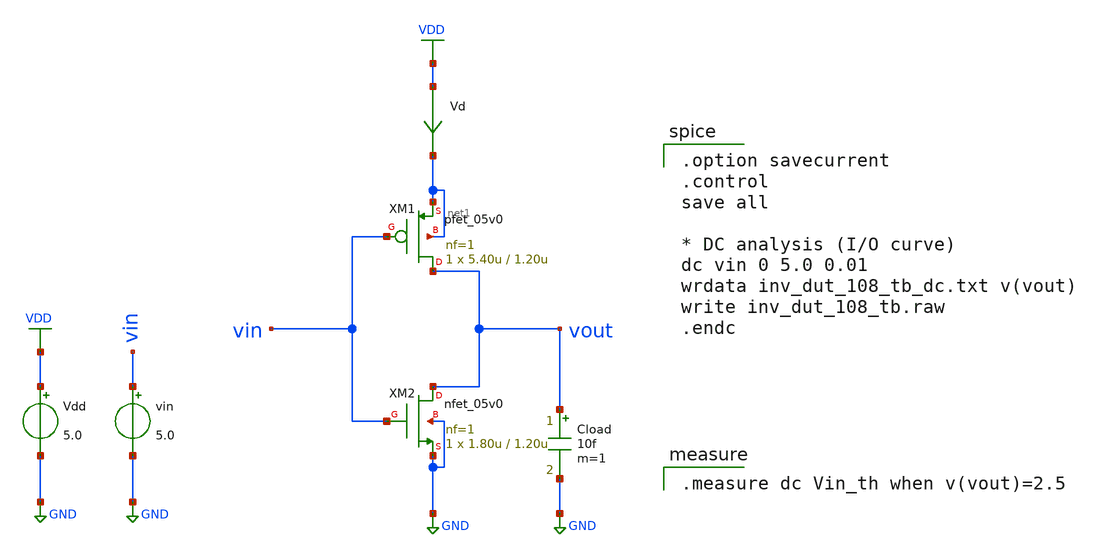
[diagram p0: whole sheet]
** sch_path: inv_dut_108_tb.sch
**.subckt inv_dut_108_tb
Vdd VDD GND 5.0
vin vin GND 5.0
Vd VDD net1 0
.save i(vd)
Cload vout GND 10f m=1
XM1 vout vin net1 net1 pfet_05v0 L=1.20u W=5.40u nf=1 ad='int((nf+1)/2) * W/nf * 0.18u' as='int((nf+2)/2) * W/nf * 0.18u'
+ pd='2*int((nf+1)/2) * (W/nf + 0.18u)' ps='2*int((nf+2)/2) * (W/nf + 0.18u)' nrd='0.18u / W' nrs='0.18u / W'
+ sa=0 sb=0 sd=0 m=1
XM2 vout vin GND GND nfet_05v0 L=1.20u W=1.80u nf=1 ad='int((nf+1)/2) * W/nf * 0.18u' as='int((nf+2)/2) * W/nf * 0.18u'
+ pd='2*int((nf+1)/2) * (W/nf + 0.18u)' ps='2*int((nf+2)/2) * (W/nf + 0.18u)' nrd='0.18u / W' nrs='0.18u / W'
+ sa=0 sb=0 sd=0 m=1
**** begin user architecture code

.option savecurrent
.control
save all

* DC analysis (I/O curve)
dc vin 0 5.0 0.01
wrdata inv_dut_108_tb_dc.txt v(vout)
write inv_dut_108_tb.raw
.endc


.measure dc Vin_th when v(vout)=2.5


.include $::180MCU_MODELS/design.ngspice
.lib $::180MCU_MODELS/sm141064.ngspice typical
.lib $::180MCU_MODELS/sm141064.ngspice res_typical
.lib $::180MCU_MODELS/sm141064.ngspice moscap_typical
.lib $::180MCU_MODELS/sm141064.ngspice diode_typical

**** end user architecture code
**.ends
.GLOBAL GND
.GLOBAL VDD
.end
